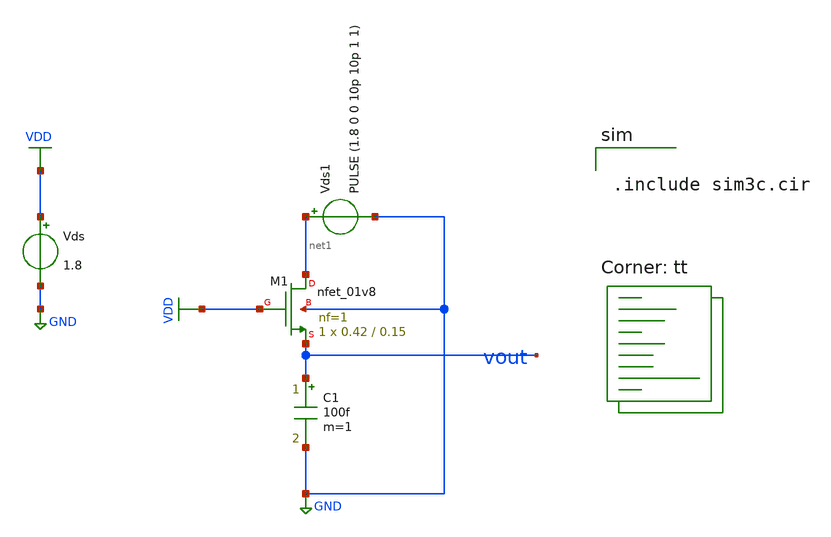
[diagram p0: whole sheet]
** sch_path: assignments/assignment1/assign3c.sch
**.subckt assign3c
XM1 net1 VDD vout GND sky130_fd_pr__nfet_01v8 L=0.15 W=0.42 nf=1 ad='int((nf+1)/2) * W/nf * 0.29' as='int((nf+2)/2) * W/nf * 0.29'
+ pd='2*int((nf+1)/2) * (W/nf + 0.29)' ps='2*int((nf+2)/2) * (W/nf + 0.29)' nrd='0.29 / W' nrs='0.29 / W'
+ sa=0 sb=0 sd=0 mult=1 m=1
Vds VDD GND 1.8
C1 vout GND 100f m=1
Vds1 net1 GND PULSE (1.8 0 0 10p 10p 1 1)
**** begin user architecture code


.include sim3c.cir


.lib $::SKYWATER_MODELS/sky130.lib.spice tt
**** end user architecture code
**.ends
.GLOBAL GND
.GLOBAL VDD
.end
